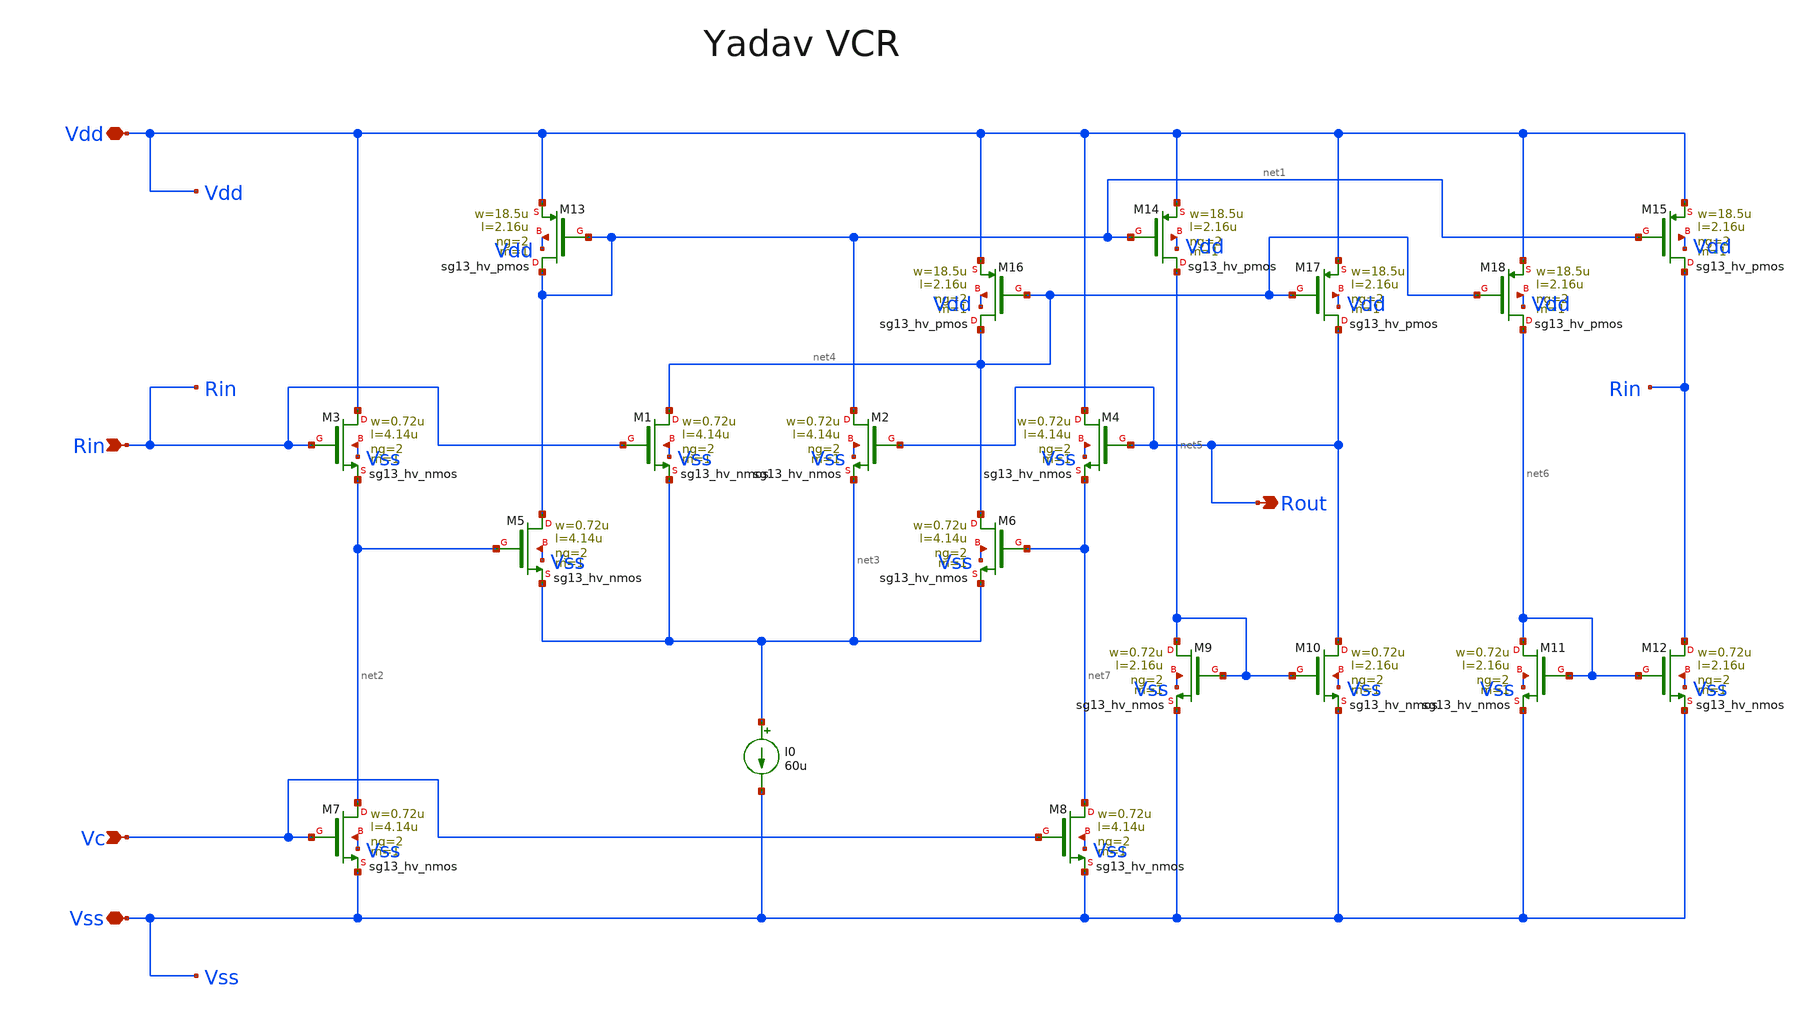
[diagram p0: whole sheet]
** sch_path: macros/heichips26_analog_project/macros/yadav/schematic/xschem/yadav.sch
**.subckt yadav Vc Vss Vdd Rin Rout
*.ipin Vc
*.iopin Vss
*.iopin Vdd
*.ipin Rin
*.opin Rout
XM3 Vdd Rin net2 Vss sg13_hv_nmos w=0.72u l=4.14u ng=2 m=1 mm_ok=1
XM13 net1 net1 Vdd Vdd sg13_hv_pmos w=18.5u l=2.16u ng=2 m=1 mm_ok=1
XM1 net4 Rin net3 Vss sg13_hv_nmos w=0.72u l=4.14u ng=2 m=1 mm_ok=1
XM5 net1 net2 net3 Vss sg13_hv_nmos w=0.72u l=4.14u ng=2 m=1 mm_ok=1
XM2 net1 Rout net3 Vss sg13_hv_nmos w=0.72u l=4.14u ng=2 m=1 mm_ok=1
XM16 net4 net4 Vdd Vdd sg13_hv_pmos w=18.5u l=2.16u ng=2 m=1 mm_ok=1
XM7 net2 Vc Vss Vss sg13_hv_nmos w=0.72u l=4.14u ng=2 m=1 mm_ok=1
XM6 net4 net7 net3 Vss sg13_hv_nmos w=0.72u l=4.14u ng=2 m=1 mm_ok=1
XM14 net5 net1 Vdd Vdd sg13_hv_pmos w=18.5u l=2.16u ng=2 m=1 mm_ok=1
XM8 net7 Vc Vss Vss sg13_hv_nmos w=0.72u l=4.14u ng=2 m=1 mm_ok=1
XM4 Vdd Rout net7 Vss sg13_hv_nmos w=0.72u l=4.14u ng=2 m=1 mm_ok=1
XM9 net5 net5 Vss Vss sg13_hv_nmos w=0.72u l=2.16u ng=2 m=1 mm_ok=1
XM10 Rout net5 Vss Vss sg13_hv_nmos w=0.72u l=2.16u ng=2 m=1 mm_ok=1
XM17 Rout net4 Vdd Vdd sg13_hv_pmos w=18.5u l=2.16u ng=2 m=1 mm_ok=1
XM18 net6 net4 Vdd Vdd sg13_hv_pmos w=18.5u l=2.16u ng=2 m=1 mm_ok=1
XM11 net6 net6 Vss Vss sg13_hv_nmos w=0.72u l=2.16u ng=2 m=1 mm_ok=1
XM12 Rin net6 Vss Vss sg13_hv_nmos w=0.72u l=2.16u ng=2 m=1 mm_ok=1
XM15 Rin net1 Vdd Vdd sg13_hv_pmos w=18.5u l=2.16u ng=2 m=1 mm_ok=1
I0 net3 Vss 60u
**.ends
.end
